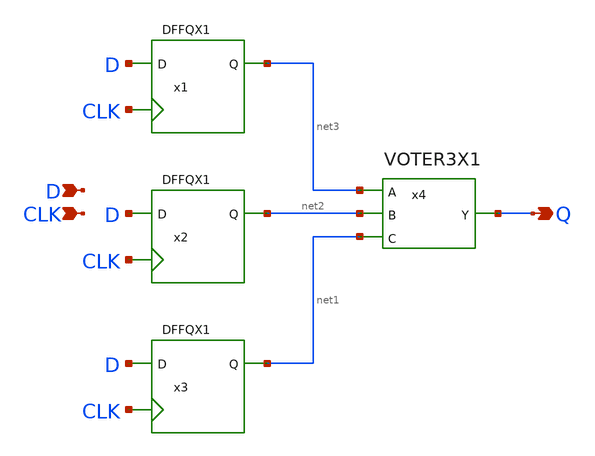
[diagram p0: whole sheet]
** sch_path: lib/xschem/TMRDFFQX1.sch
**.subckt TMRDFFQX1 Q D CLK
*.opin Q
*.ipin D
*.ipin CLK
x1 CLK net3 D VDD VSS DFFQX1
x2 CLK net2 D VDD VSS DFFQX1
x3 CLK net1 D VDD VSS DFFQX1
x4 net3 net2 net1 Q VDD VSS VOTER3X1
**.ends

* expanding   symbol:  DFFQX1.sym # of pins=3
** sym_path: DFFQX1.sym
** sch_path: DFFQX1.sch
.subckt DFFQX1 CLK Q D VDD VSS
*.ipin CLK
*.ipin D
*.opin Q
x1 B1 C1 CLK A1 NAND3X1
x2 A1 B1 D NAND2X1
x3 D1 A1 C1 NAND2X1
x4 C1 D1 CLK NAND2X1
x5 net1 B1 Q NAND2X1
x6 Q net1 C1 NAND2X1
.ends


* expanding   symbol:  VOTER3X1.sym # of pins=4
** sym_path: lib/xschem/VOTER3X1.sym
** sch_path: lib/xschem/VOTER3X1.sch
.subckt VOTER3X1 A B C Y VDD VSS
*.opin Y
*.ipin A
*.ipin B
*.ipin C
x1 Y net1 INVX1
x2 A B C net1 VDD VSS VOTERN3X1
.ends


* expanding   symbol:  NAND3X1.sym # of pins=4
** sym_path: lib/xschem/NAND3X1.sym
** sch_path: lib/xschem/NAND3X1.sch
.subckt NAND3X1 Y A B C
*.opin Y
*.ipin A
*.ipin B
*.ipin C
XM1 net2 A VSS VSS sky130_fd_pr__nfet_01v8 L=0.15 W=3 nf=1 ad='int((nf+1)/2) * W/nf * 0.29' as='int((nf+2)/2) * W/nf * 0.29'
+ pd='2*int((nf+1)/2) * (W/nf + 0.29)' ps='2*int((nf+2)/2) * (W/nf + 0.29)' nrd='0.29 / W' nrs='0.29 / W'
+ sa=0 sb=0 sd=0 mult=1 m=1
XM2 Y A VDD VDD sky130_fd_pr__pfet_01v8 L=0.15 W=nf=1 nf=1 ad='int((nf+1)/2) * W/nf * 0.29' as='int((nf+2)/2) * W/nf * 0.29'
+ pd='2*int((nf+1)/2) * (W/nf + 0.29)' ps='2*int((nf+2)/2) * (W/nf + 0.29)' nrd='0.29 / W' nrs='0.29 / W'
+ sa=0 sb=0 sd=0 mult=2 m=2
XM3 net1 B net2 VSS sky130_fd_pr__nfet_01v8 L=0.15 W=3 nf=1 ad='int((nf+1)/2) * W/nf * 0.29' as='int((nf+2)/2) * W/nf * 0.29'
+ pd='2*int((nf+1)/2) * (W/nf + 0.29)' ps='2*int((nf+2)/2) * (W/nf + 0.29)' nrd='0.29 / W' nrs='0.29 / W'
+ sa=0 sb=0 sd=0 mult=1 m=1
XM4 Y C net1 VSS sky130_fd_pr__nfet_01v8 L=0.15 W=3 nf=1 ad='int((nf+1)/2) * W/nf * 0.29' as='int((nf+2)/2) * W/nf * 0.29'
+ pd='2*int((nf+1)/2) * (W/nf + 0.29)' ps='2*int((nf+2)/2) * (W/nf + 0.29)' nrd='0.29 / W' nrs='0.29 / W'
+ sa=0 sb=0 sd=0 mult=1 m=1
XM5 Y B VDD VDD sky130_fd_pr__pfet_01v8 L=0.15 W=nf=1 nf=1 ad='int((nf+1)/2) * W/nf * 0.29' as='int((nf+2)/2) * W/nf * 0.29'
+ pd='2*int((nf+1)/2) * (W/nf + 0.29)' ps='2*int((nf+2)/2) * (W/nf + 0.29)' nrd='0.29 / W' nrs='0.29 / W'
+ sa=0 sb=0 sd=0 mult=2 m=2
XM6 Y C VDD VDD sky130_fd_pr__pfet_01v8 L=0.15 W=nf=1 nf=1 ad='int((nf+1)/2) * W/nf * 0.29' as='int((nf+2)/2) * W/nf * 0.29'
+ pd='2*int((nf+1)/2) * (W/nf + 0.29)' ps='2*int((nf+2)/2) * (W/nf + 0.29)' nrd='0.29 / W' nrs='0.29 / W'
+ sa=0 sb=0 sd=0 mult=2 m=2
.ends


* expanding   symbol:  NAND2X1.sym # of pins=3
** sym_path: lib/xschem/NAND2X1.sym
** sch_path: lib/xschem/NAND2X1.sch
.subckt NAND2X1 Y A B
*.ipin A
*.opin Y
*.ipin B
XM1 Y A VDD VDD sky130_fd_pr__pfet_01v8 L=0.15 W=2 nf=1 ad='int((nf+1)/2) * W/nf * 0.29' as='int((nf+2)/2) * W/nf * 0.29'
+ pd='2*int((nf+1)/2) * (W/nf + 0.29)' ps='2*int((nf+2)/2) * (W/nf + 0.29)' nrd='0.29 / W' nrs='0.29 / W'
+ sa=0 sb=0 sd=0 mult=1 m=1
XM5 Y A net1 VSS sky130_fd_pr__nfet_01v8 L=0.15 W=3 nf=1 ad='int((nf+1)/2) * W/nf * 0.29' as='int((nf+2)/2) * W/nf * 0.29'
+ pd='2*int((nf+1)/2) * (W/nf + 0.29)' ps='2*int((nf+2)/2) * (W/nf + 0.29)' nrd='0.29 / W' nrs='0.29 / W'
+ sa=0 sb=0 sd=0 mult=1 m=1
XM2 Y A VDD VDD sky130_fd_pr__pfet_01v8 L=0.15 W=2 nf=1 ad='int((nf+1)/2) * W/nf * 0.29' as='int((nf+2)/2) * W/nf * 0.29'
+ pd='2*int((nf+1)/2) * (W/nf + 0.29)' ps='2*int((nf+2)/2) * (W/nf + 0.29)' nrd='0.29 / W' nrs='0.29 / W'
+ sa=0 sb=0 sd=0 mult=1 m=1
XM3 Y B VDD VDD sky130_fd_pr__pfet_01v8 L=0.15 W=2 nf=1 ad='int((nf+1)/2) * W/nf * 0.29' as='int((nf+2)/2) * W/nf * 0.29'
+ pd='2*int((nf+1)/2) * (W/nf + 0.29)' ps='2*int((nf+2)/2) * (W/nf + 0.29)' nrd='0.29 / W' nrs='0.29 / W'
+ sa=0 sb=0 sd=0 mult=1 m=1
XM4 Y B VDD VDD sky130_fd_pr__pfet_01v8 L=0.15 W=2 nf=1 ad='int((nf+1)/2) * W/nf * 0.29' as='int((nf+2)/2) * W/nf * 0.29'
+ pd='2*int((nf+1)/2) * (W/nf + 0.29)' ps='2*int((nf+2)/2) * (W/nf + 0.29)' nrd='0.29 / W' nrs='0.29 / W'
+ sa=0 sb=0 sd=0 mult=1 m=1
XM6 net1 B VSS VSS sky130_fd_pr__nfet_01v8 L=0.15 W=3 nf=1 ad='int((nf+1)/2) * W/nf * 0.29' as='int((nf+2)/2) * W/nf * 0.29'
+ pd='2*int((nf+1)/2) * (W/nf + 0.29)' ps='2*int((nf+2)/2) * (W/nf + 0.29)' nrd='0.29 / W' nrs='0.29 / W'
+ sa=0 sb=0 sd=0 mult=1 m=1
.ends


* expanding   symbol:  VOTERN3X1.sym # of pins=4
** sym_path: VOTERN3X1.sym
** sch_path: VOTERN3X1.sch
.subckt VOTERN3X1 A B C YN VDD VSS
*.opin YN
*.ipin A
*.ipin B
*.ipin C
XM2 net1 A VDD VDD sky130_fd_pr__pfet_01v8 L=0.15 W=2 nf=1 ad='int((nf+1)/2) * W/nf * 0.29' as='int((nf+2)/2) * W/nf * 0.29'
+ pd='2*int((nf+1)/2) * (W/nf + 0.29)' ps='2*int((nf+2)/2) * (W/nf + 0.29)' nrd='0.29 / W' nrs='0.29 / W'
+ sa=0 sb=0 sd=0 mult=2 m=2
XM3 net2 B VSS VSS sky130_fd_pr__nfet_01v8 L=0.15 W=3 nf=1 ad='int((nf+1)/2) * W/nf * 0.29' as='int((nf+2)/2) * W/nf * 0.29'
+ pd='2*int((nf+1)/2) * (W/nf + 0.29)' ps='2*int((nf+2)/2) * (W/nf + 0.29)' nrd='0.29 / W' nrs='0.29 / W'
+ sa=0 sb=0 sd=0 mult=1 m=1
XM4 YN A net2 VSS sky130_fd_pr__nfet_01v8 L=0.15 W=3 nf=1 ad='int((nf+1)/2) * W/nf * 0.29' as='int((nf+2)/2) * W/nf * 0.29'
+ pd='2*int((nf+1)/2) * (W/nf + 0.29)' ps='2*int((nf+2)/2) * (W/nf + 0.29)' nrd='0.29 / W' nrs='0.29 / W'
+ sa=0 sb=0 sd=0 mult=1 m=1
XM1 net1 B VDD VDD sky130_fd_pr__pfet_01v8 L=0.15 W=2 nf=1 ad='int((nf+1)/2) * W/nf * 0.29' as='int((nf+2)/2) * W/nf * 0.29'
+ pd='2*int((nf+1)/2) * (W/nf + 0.29)' ps='2*int((nf+2)/2) * (W/nf + 0.29)' nrd='0.29 / W' nrs='0.29 / W'
+ sa=0 sb=0 sd=0 mult=2 m=2
XM5 net3 B net1 VDD sky130_fd_pr__pfet_01v8 L=0.15 W=2 nf=1 ad='int((nf+1)/2) * W/nf * 0.29' as='int((nf+2)/2) * W/nf * 0.29'
+ pd='2*int((nf+1)/2) * (W/nf + 0.29)' ps='2*int((nf+2)/2) * (W/nf + 0.29)' nrd='0.29 / W' nrs='0.29 / W'
+ sa=0 sb=0 sd=0 mult=2 m=2
XM6 YN C net3 VDD sky130_fd_pr__pfet_01v8 L=0.15 W=2 nf=1 ad='int((nf+1)/2) * W/nf * 0.29' as='int((nf+2)/2) * W/nf * 0.29'
+ pd='2*int((nf+1)/2) * (W/nf + 0.29)' ps='2*int((nf+2)/2) * (W/nf + 0.29)' nrd='0.29 / W' nrs='0.29 / W'
+ sa=0 sb=0 sd=0 mult=2 m=2
XM7 net3 C net1 VDD sky130_fd_pr__pfet_01v8 L=0.15 W=2 nf=1 ad='int((nf+1)/2) * W/nf * 0.29' as='int((nf+2)/2) * W/nf * 0.29'
+ pd='2*int((nf+1)/2) * (W/nf + 0.29)' ps='2*int((nf+2)/2) * (W/nf + 0.29)' nrd='0.29 / W' nrs='0.29 / W'
+ sa=0 sb=0 sd=0 mult=2 m=2
XM10 YN A net3 VDD sky130_fd_pr__pfet_01v8 L=0.15 W=2 nf=1 ad='int((nf+1)/2) * W/nf * 0.29' as='int((nf+2)/2) * W/nf * 0.29'
+ pd='2*int((nf+1)/2) * (W/nf + 0.29)' ps='2*int((nf+2)/2) * (W/nf + 0.29)' nrd='0.29 / W' nrs='0.29 / W'
+ sa=0 sb=0 sd=0 mult=2 m=2
XM8 net4 B VSS VSS sky130_fd_pr__nfet_01v8 L=0.15 W=3 nf=1 ad='int((nf+1)/2) * W/nf * 0.29' as='int((nf+2)/2) * W/nf * 0.29'
+ pd='2*int((nf+1)/2) * (W/nf + 0.29)' ps='2*int((nf+2)/2) * (W/nf + 0.29)' nrd='0.29 / W' nrs='0.29 / W'
+ sa=0 sb=0 sd=0 mult=1 m=1
XM9 YN C net4 VSS sky130_fd_pr__nfet_01v8 L=0.15 W=3 nf=1 ad='int((nf+1)/2) * W/nf * 0.29' as='int((nf+2)/2) * W/nf * 0.29'
+ pd='2*int((nf+1)/2) * (W/nf + 0.29)' ps='2*int((nf+2)/2) * (W/nf + 0.29)' nrd='0.29 / W' nrs='0.29 / W'
+ sa=0 sb=0 sd=0 mult=1 m=1
XM11 net5 C VSS VSS sky130_fd_pr__nfet_01v8 L=0.15 W=3 nf=1 ad='int((nf+1)/2) * W/nf * 0.29' as='int((nf+2)/2) * W/nf * 0.29'
+ pd='2*int((nf+1)/2) * (W/nf + 0.29)' ps='2*int((nf+2)/2) * (W/nf + 0.29)' nrd='0.29 / W' nrs='0.29 / W'
+ sa=0 sb=0 sd=0 mult=1 m=1
XM12 YN A net5 VSS sky130_fd_pr__nfet_01v8 L=0.15 W=3 nf=1 ad='int((nf+1)/2) * W/nf * 0.29' as='int((nf+2)/2) * W/nf * 0.29'
+ pd='2*int((nf+1)/2) * (W/nf + 0.29)' ps='2*int((nf+2)/2) * (W/nf + 0.29)' nrd='0.29 / W' nrs='0.29 / W'
+ sa=0 sb=0 sd=0 mult=1 m=1
.ends

.end
